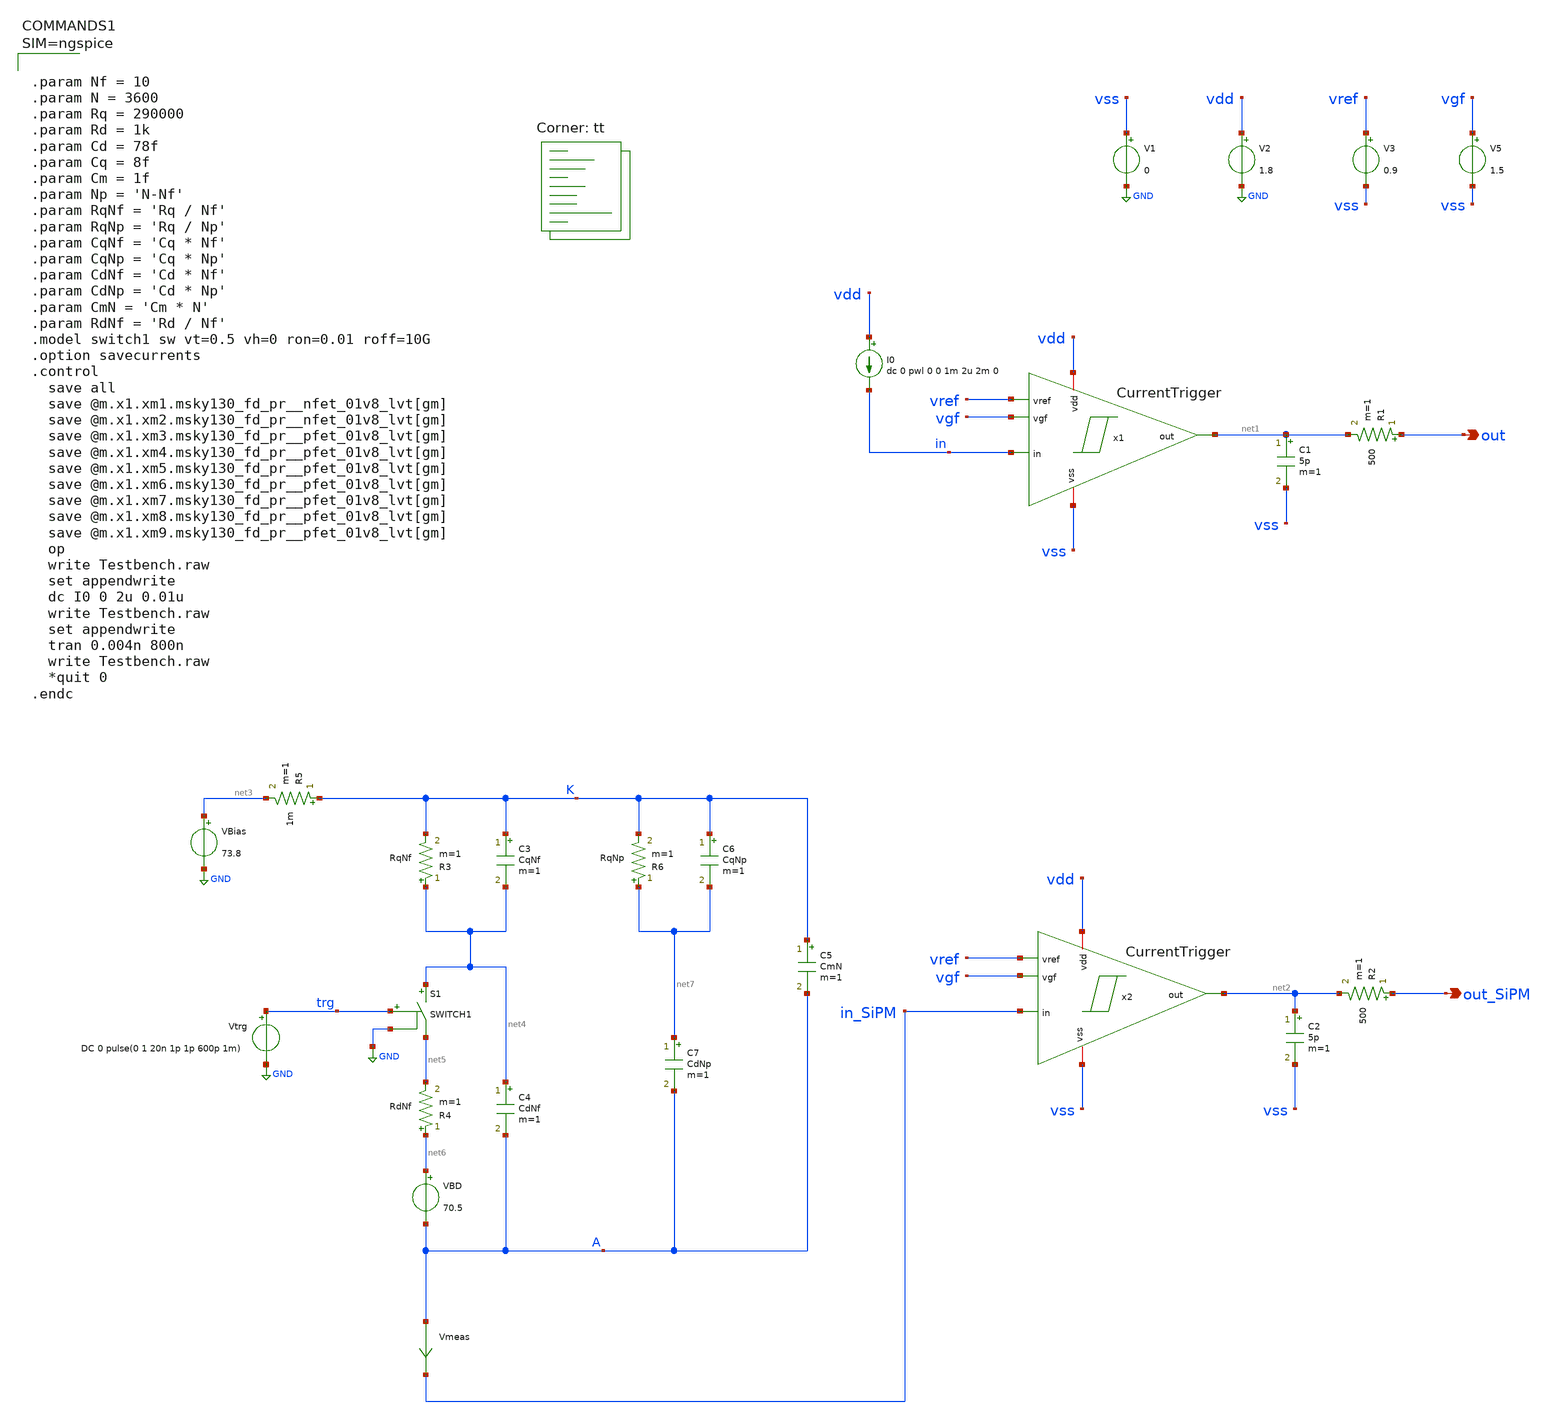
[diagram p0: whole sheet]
** sch_path: xschem/Testbench.sch
**.subckt Testbench out out_SiPM
*.opin out
*.opin out_SiPM
x1 vdd vss vref vgf net1 in CurrentTrigger
V1 vss GND 0
.save i(v1)
V2 vdd GND 1.8
.save i(v2)
C1 net1 vss 5p m=1
R1 out net1 500 m=1
V3 vref vss 0.9
.save i(v3)
V5 vgf vss 1.5
.save i(v5)
I0 vdd in dc 0 pwl 0 0 1m 2u 2m 0
x2 vdd vss vref vgf net2 in_SiPM CurrentTrigger
C2 net2 vss 5p m=1
R2 out_SiPM net2 500 m=1
R5 K net3 1m m=1
R3 net4 K RqNf m=1
R4 net6 net5 RdNf m=1
VBD net6 A 70.5
C3 K net4 CqNf m=1
C4 net4 A CdNf m=1
R6 net7 K RqNp m=1
C5 K A CmN m=1
C6 K net7 CqNp m=1
C7 net7 A CdNp m=1
VBias net3 GND 73.8
Vtrg trg GND DC 0 pulse(0 1 20n 1p 1p 600p 1m)
S1 net4 net5 trg GND SWITCH1
Vmeas A in_SiPM 0
.save i(vmeas)
**** begin user architecture code



.param Nf = 10
.param N = 3600
.param Rq = 290000
.param Rd = 1k
.param Cd = 78f
.param Cq = 8f
.param Cm = 1f
.param Np = 'N-Nf'
.param RqNf = 'Rq / Nf'
.param RqNp = 'Rq / Np'
.param CqNf = 'Cq * Nf'
.param CqNp = 'Cq * Np'
.param CdNf = 'Cd * Nf'
.param CdNp = 'Cd * Np'
.param CmN = 'Cm * N'
.param RdNf = 'Rd / Nf'
.model switch1 sw vt=0.5 vh=0 ron=0.01 roff=10G
.option savecurrents
.control
  save all
  save @m.x1.xm1.msky130_fd_pr__nfet_01v8_lvt[gm]
  save @m.x1.xm2.msky130_fd_pr__nfet_01v8_lvt[gm]
  save @m.x1.xm3.msky130_fd_pr__pfet_01v8_lvt[gm]
  save @m.x1.xm4.msky130_fd_pr__pfet_01v8_lvt[gm]
  save @m.x1.xm5.msky130_fd_pr__pfet_01v8_lvt[gm]
  save @m.x1.xm6.msky130_fd_pr__pfet_01v8_lvt[gm]
  save @m.x1.xm7.msky130_fd_pr__pfet_01v8_lvt[gm]
  save @m.x1.xm8.msky130_fd_pr__pfet_01v8_lvt[gm]
  save @m.x1.xm9.msky130_fd_pr__pfet_01v8_lvt[gm]
  op
  write Testbench.raw
  set appendwrite
  dc I0 0 2u 0.01u
  write Testbench.raw
  set appendwrite
  tran 0.004n 800n
  write Testbench.raw
  *quit 0
.endc



.lib $::SKYWATER_MODELS/sky130.lib.spice tt
**** end user architecture code
**.ends

* expanding   symbol:  CurrentTrigger.sym # of pins=6
** sym_path: xschem/CurrentTrigger.sym
** sch_path: xschem/CurrentTrigger.sch
.subckt CurrentTrigger vdd vss vref vgf out in
*.iopin vdd
*.iopin vss
*.ipin in
*.opin out
*.ipin vref
*.ipin vgf
XM1 out1 g2 vss vss sky130_fd_pr__nfet_01v8_lvt L=1 W=3 nf=3 ad='int((nf+1)/2) * W/nf * 0.29' as='int((nf+2)/2) * W/nf * 0.29'
+ pd='2*int((nf+1)/2) * (W/nf + 0.29)' ps='2*int((nf+2)/2) * (W/nf + 0.29)' nrd='0.29 / W' nrs='0.29 / W'
+ sa=0 sb=0 sd=0 mult=1 m=1
XM2 g2 g2 vss vss sky130_fd_pr__nfet_01v8_lvt L=1 W=3 nf=3 ad='int((nf+1)/2) * W/nf * 0.29' as='int((nf+2)/2) * W/nf * 0.29'
+ pd='2*int((nf+1)/2) * (W/nf + 0.29)' ps='2*int((nf+2)/2) * (W/nf + 0.29)' nrd='0.29 / W' nrs='0.29 / W'
+ sa=0 sb=0 sd=0 mult=1 m=1
XM3 g2 vm in vdd sky130_fd_pr__pfet_01v8_lvt L=0.35 W=15 nf=1 ad='int((nf+1)/2) * W/nf * 0.29' as='int((nf+2)/2) * W/nf * 0.29'
+ pd='2*int((nf+1)/2) * (W/nf + 0.29)' ps='2*int((nf+2)/2) * (W/nf + 0.29)' nrd='0.29 / W' nrs='0.29 / W'
+ sa=0 sb=0 sd=0 mult=1 m=1
XM4 g1 g1 in vdd sky130_fd_pr__pfet_01v8_lvt L=0.7 W=27 nf=18 ad='int((nf+1)/2) * W/nf * 0.29' as='int((nf+2)/2) * W/nf * 0.29'
+ pd='2*int((nf+1)/2) * (W/nf + 0.29)' ps='2*int((nf+2)/2) * (W/nf + 0.29)' nrd='0.29 / W' nrs='0.29 / W'
+ sa=0 sb=0 sd=0 mult=1 m=1
XM5 vm g1 vref vdd sky130_fd_pr__pfet_01v8_lvt L=0.7 W=27 nf=18 ad='int((nf+1)/2) * W/nf * 0.29' as='int((nf+2)/2) * W/nf * 0.29'
+ pd='2*int((nf+1)/2) * (W/nf + 0.29)' ps='2*int((nf+2)/2) * (W/nf + 0.29)' nrd='0.29 / W' nrs='0.29 / W'
+ sa=0 sb=0 sd=0 mult=1 m=1
XM6 in vgb vdd vdd sky130_fd_pr__pfet_01v8_lvt L=3 W=18 nf=9 ad='int((nf+1)/2) * W/nf * 0.29' as='int((nf+2)/2) * W/nf * 0.29'
+ pd='2*int((nf+1)/2) * (W/nf + 0.29)' ps='2*int((nf+2)/2) * (W/nf + 0.29)' nrd='0.29 / W' nrs='0.29 / W'
+ sa=0 sb=0 sd=0 mult=1 m=1
XM7 net1 out3 vdd vdd sky130_fd_pr__pfet_01v8_lvt L=0.35 W=5 nf=5 ad='int((nf+1)/2) * W/nf * 0.29' as='int((nf+2)/2) * W/nf * 0.29'
+ pd='2*int((nf+1)/2) * (W/nf + 0.29)' ps='2*int((nf+2)/2) * (W/nf + 0.29)' nrd='0.29 / W' nrs='0.29 / W'
+ sa=0 sb=0 sd=0 mult=1 m=1
XM9 out1 vgb vdd vdd sky130_fd_pr__pfet_01v8_lvt L=3 W=12 nf=6 ad='int((nf+1)/2) * W/nf * 0.29' as='int((nf+2)/2) * W/nf * 0.29'
+ pd='2*int((nf+1)/2) * (W/nf + 0.29)' ps='2*int((nf+2)/2) * (W/nf + 0.29)' nrd='0.29 / W' nrs='0.29 / W'
+ sa=0 sb=0 sd=0 mult=1 m=1
XM10 out2 out1 vss vss sky130_fd_pr__nfet_01v8_lvt L=0.15 W=1 nf=1 ad='int((nf+1)/2) * W/nf * 0.29' as='int((nf+2)/2) * W/nf * 0.29'
+ pd='2*int((nf+1)/2) * (W/nf + 0.29)' ps='2*int((nf+2)/2) * (W/nf + 0.29)' nrd='0.29 / W' nrs='0.29 / W'
+ sa=0 sb=0 sd=0 mult=1 m=1
XM11 out2 out1 vdd vdd sky130_fd_pr__pfet_01v8_lvt L=0.35 W=2 nf=1 ad='int((nf+1)/2) * W/nf * 0.29' as='int((nf+2)/2) * W/nf * 0.29'
+ pd='2*int((nf+1)/2) * (W/nf + 0.29)' ps='2*int((nf+2)/2) * (W/nf + 0.29)' nrd='0.29 / W' nrs='0.29 / W'
+ sa=0 sb=0 sd=0 mult=1 m=1
XM12 out3 out2 vdd vdd sky130_fd_pr__pfet_01v8_lvt L=0.35 W=6 nf=1 ad='int((nf+1)/2) * W/nf * 0.29' as='int((nf+2)/2) * W/nf * 0.29'
+ pd='2*int((nf+1)/2) * (W/nf + 0.29)' ps='2*int((nf+2)/2) * (W/nf + 0.29)' nrd='0.29 / W' nrs='0.29 / W'
+ sa=0 sb=0 sd=0 mult=1 m=1
XM13 out3 out2 vss vss sky130_fd_pr__nfet_01v8_lvt L=0.15 W=3 nf=1 ad='int((nf+1)/2) * W/nf * 0.29' as='int((nf+2)/2) * W/nf * 0.29'
+ pd='2*int((nf+1)/2) * (W/nf + 0.29)' ps='2*int((nf+2)/2) * (W/nf + 0.29)' nrd='0.29 / W' nrs='0.29 / W'
+ sa=0 sb=0 sd=0 mult=1 m=1
XM14 out out3 vdd vdd sky130_fd_pr__pfet_01v8_lvt L=0.35 W=18 nf=1 ad='int((nf+1)/2) * W/nf * 0.29' as='int((nf+2)/2) * W/nf * 0.29'
+ pd='2*int((nf+1)/2) * (W/nf + 0.29)' ps='2*int((nf+2)/2) * (W/nf + 0.29)' nrd='0.29 / W' nrs='0.29 / W'
+ sa=0 sb=0 sd=0 mult=1 m=1
XM15 out out3 vss vss sky130_fd_pr__nfet_01v8_lvt L=0.15 W=9 nf=1 ad='int((nf+1)/2) * W/nf * 0.29' as='int((nf+2)/2) * W/nf * 0.29'
+ pd='2*int((nf+1)/2) * (W/nf + 0.29)' ps='2*int((nf+2)/2) * (W/nf + 0.29)' nrd='0.29 / W' nrs='0.29 / W'
+ sa=0 sb=0 sd=0 mult=1 m=1
XM16 g1 i_n vss vss sky130_fd_pr__nfet_01v8_lvt L=3 W=12 nf=3 ad='int((nf+1)/2) * W/nf * 0.29' as='int((nf+2)/2) * W/nf * 0.29'
+ pd='2*int((nf+1)/2) * (W/nf + 0.29)' ps='2*int((nf+2)/2) * (W/nf + 0.29)' nrd='0.29 / W' nrs='0.29 / W'
+ sa=0 sb=0 sd=0 mult=1 m=1
XM17 vm i_n vss vss sky130_fd_pr__nfet_01v8_lvt L=3 W=12 nf=3 ad='int((nf+1)/2) * W/nf * 0.29' as='int((nf+2)/2) * W/nf * 0.29'
+ pd='2*int((nf+1)/2) * (W/nf + 0.29)' ps='2*int((nf+2)/2) * (W/nf + 0.29)' nrd='0.29 / W' nrs='0.29 / W'
+ sa=0 sb=0 sd=0 mult=1 m=1
XM18 i_n i_n vss vss sky130_fd_pr__nfet_01v8_lvt L=3 W=3 nf=1 ad='int((nf+1)/2) * W/nf * 0.29' as='int((nf+2)/2) * W/nf * 0.29'
+ pd='2*int((nf+1)/2) * (W/nf + 0.29)' ps='2*int((nf+2)/2) * (W/nf + 0.29)' nrd='0.29 / W' nrs='0.29 / W'
+ sa=0 sb=0 sd=0 mult=1 m=1
XM19 vgb vgb vdd vdd sky130_fd_pr__pfet_01v8_lvt L=3 W=3 nf=1 ad='int((nf+1)/2) * W/nf * 0.29' as='int((nf+2)/2) * W/nf * 0.29'
+ pd='2*int((nf+1)/2) * (W/nf + 0.29)' ps='2*int((nf+2)/2) * (W/nf + 0.29)' nrd='0.29 / W' nrs='0.29 / W'
+ sa=0 sb=0 sd=0 mult=1 m=1
XM20 dcon dcon i_n vss sky130_fd_pr__nfet_01v8_lvt L=0.15 W=21 nf=1 ad='int((nf+1)/2) * W/nf * 0.29'
+ as='int((nf+2)/2) * W/nf * 0.29' pd='2*int((nf+1)/2) * (W/nf + 0.29)' ps='2*int((nf+2)/2) * (W/nf + 0.29)'
+ nrd='0.29 / W' nrs='0.29 / W' sa=0 sb=0 sd=0 mult=1 m=1
XM21 dcon dcon vgb vdd sky130_fd_pr__pfet_01v8_lvt L=0.35 W=21 nf=1 ad='int((nf+1)/2) * W/nf * 0.29'
+ as='int((nf+2)/2) * W/nf * 0.29' pd='2*int((nf+1)/2) * (W/nf + 0.29)' ps='2*int((nf+2)/2) * (W/nf + 0.29)'
+ nrd='0.29 / W' nrs='0.29 / W' sa=0 sb=0 sd=0 mult=1 m=1
XM8 net1 vgf in vss sky130_fd_pr__nfet_01v8_lvt L=2 W=3 nf=3 ad='int((nf+1)/2) * W/nf * 0.29' as='int((nf+2)/2) * W/nf * 0.29'
+ pd='2*int((nf+1)/2) * (W/nf + 0.29)' ps='2*int((nf+2)/2) * (W/nf + 0.29)' nrd='0.29 / W' nrs='0.29 / W'
+ sa=0 sb=0 sd=0 mult=1 m=1
.ends

.GLOBAL GND
.end
